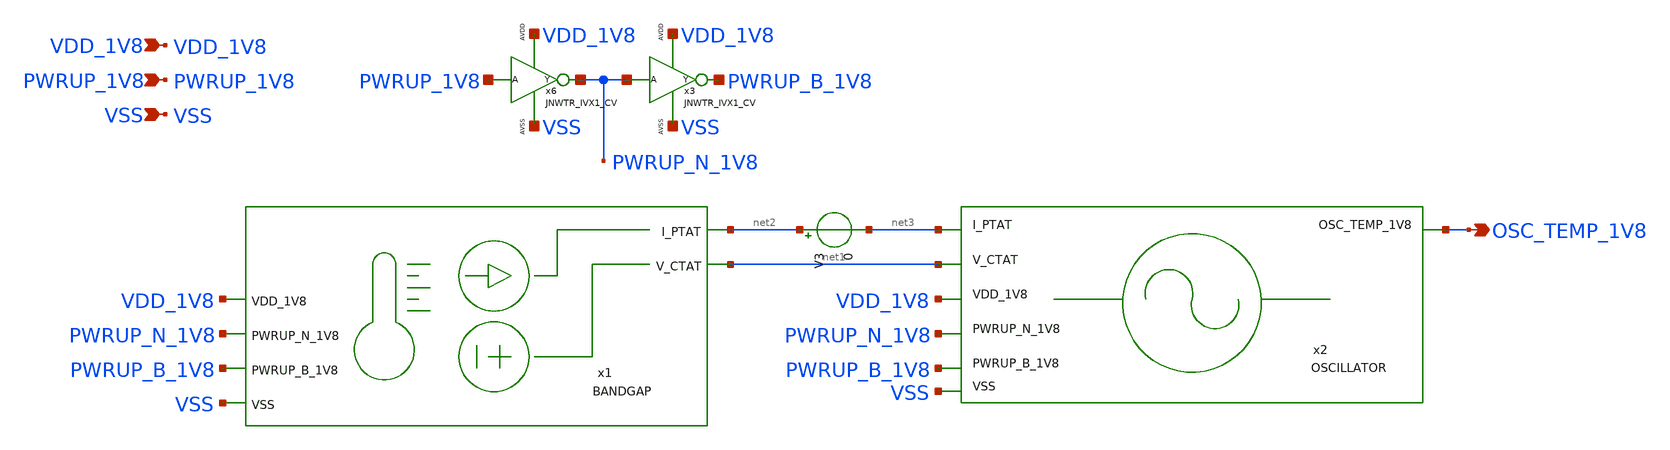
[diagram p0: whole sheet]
** sch_path: design/LELO_GR02_SKY130A/LELO_GR02.sch
**.subckt LELO_GR02 VSS PWRUP_1V8 OSC_TEMP_1V8 VDD_1V8
*.ipin VSS
*.ipin PWRUP_1V8
*.opin OSC_TEMP_1V8
*.ipin VDD_1V8
x1 VDD_1V8 net2 net1 PWRUP_N_1V8 VSS PWRUP_B_1V8 BANDGAP
x2 OSC_TEMP_1V8 VDD_1V8 PWRUP_N_1V8 VSS net1 net3 PWRUP_B_1V8 OSCILLATOR
x6 PWRUP_1V8 PWRUP_N_1V8 VDD_1V8 VSS JNWTR_IVX1_CV
x3 PWRUP_N_1V8 PWRUP_B_1V8 VDD_1V8 VSS JNWTR_IVX1_CV
V3 net2 net3 0
**.ends
.end
